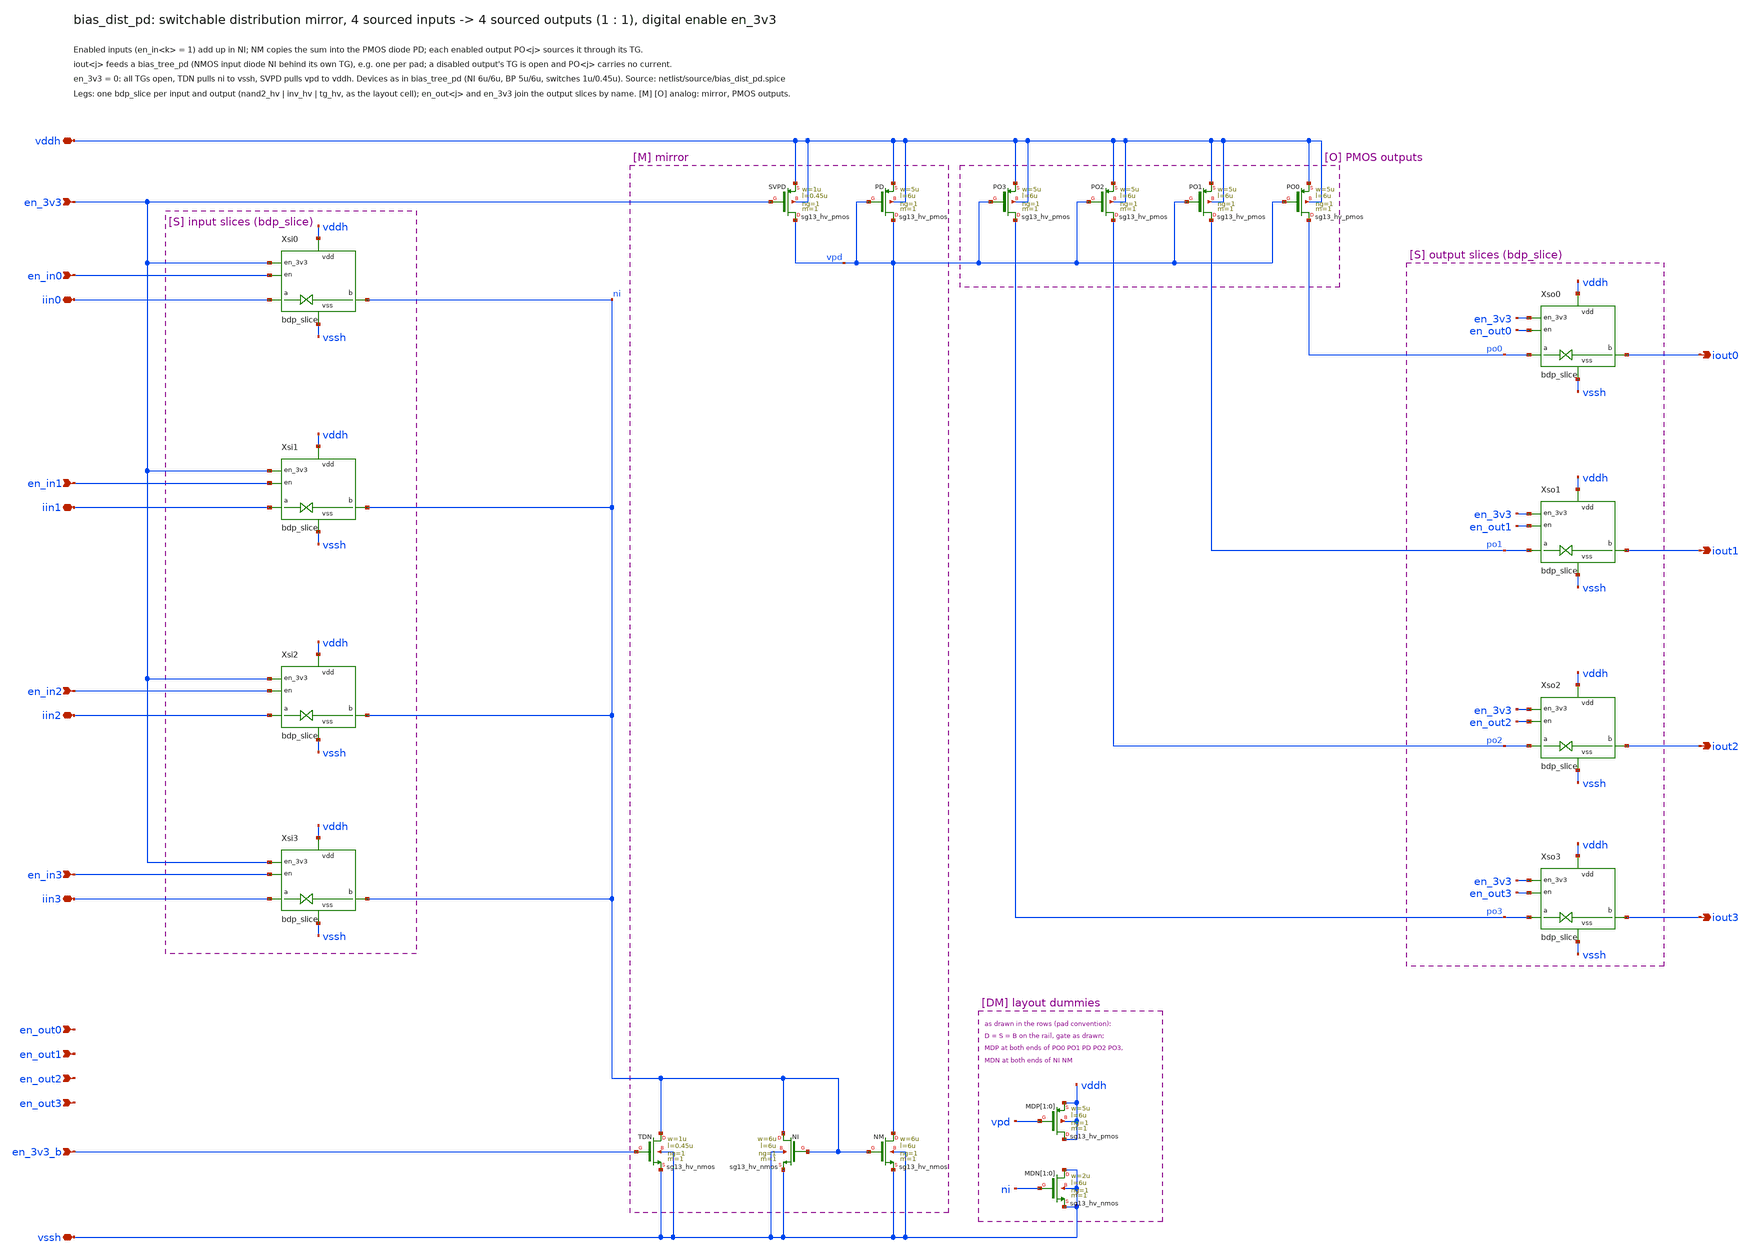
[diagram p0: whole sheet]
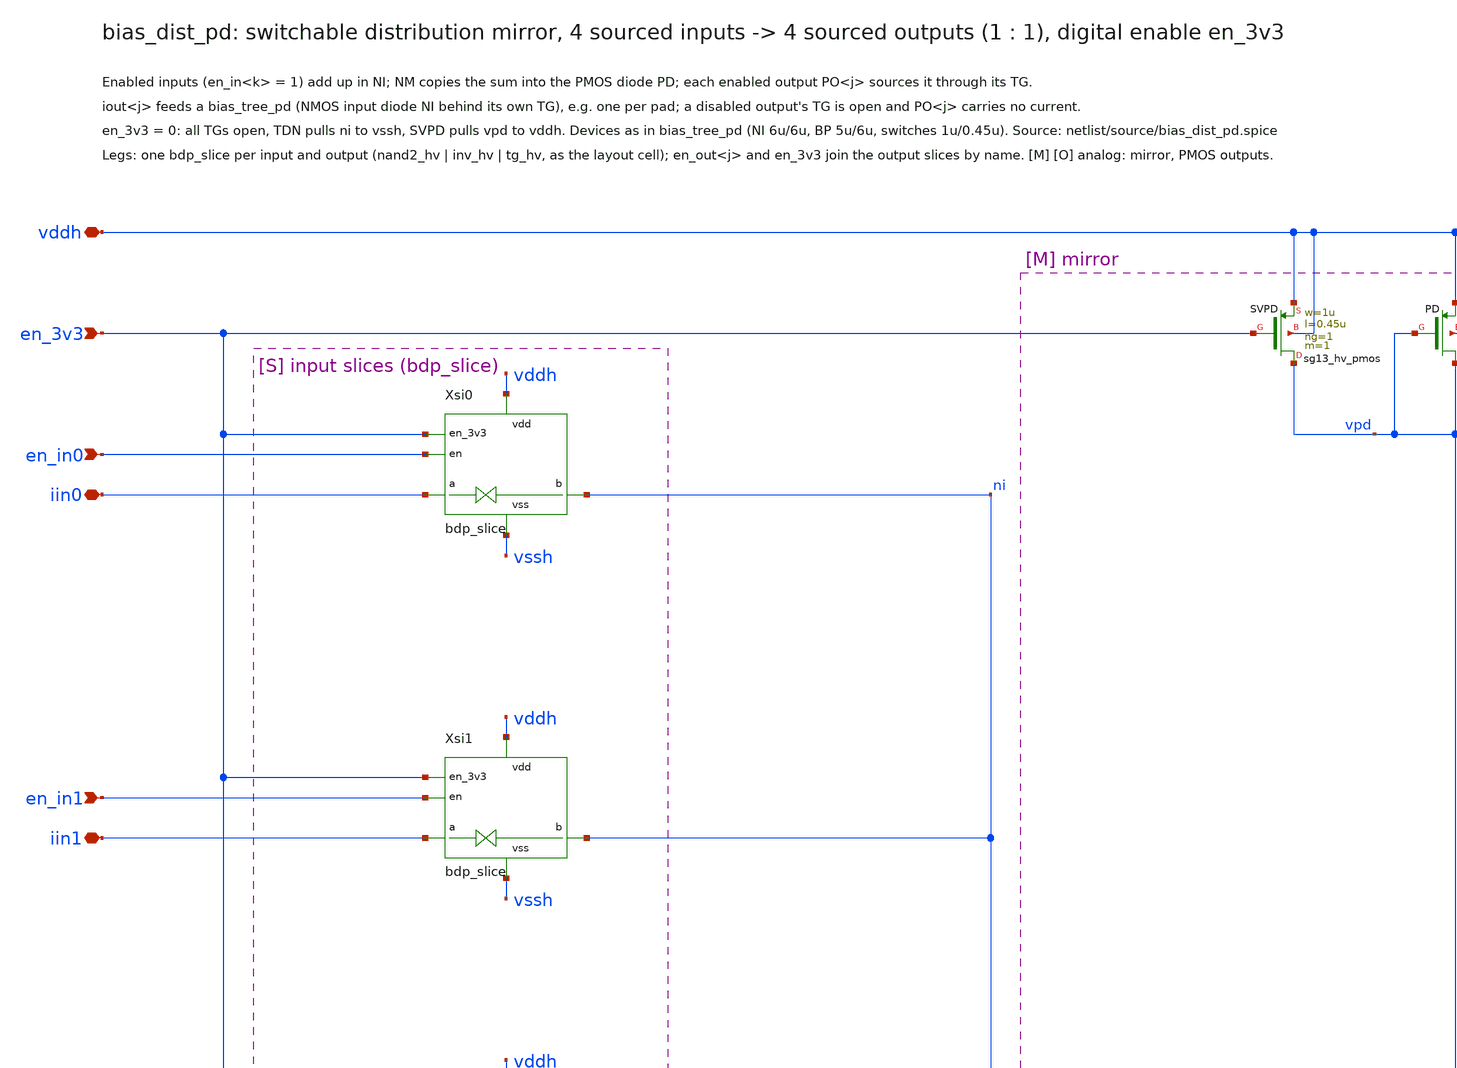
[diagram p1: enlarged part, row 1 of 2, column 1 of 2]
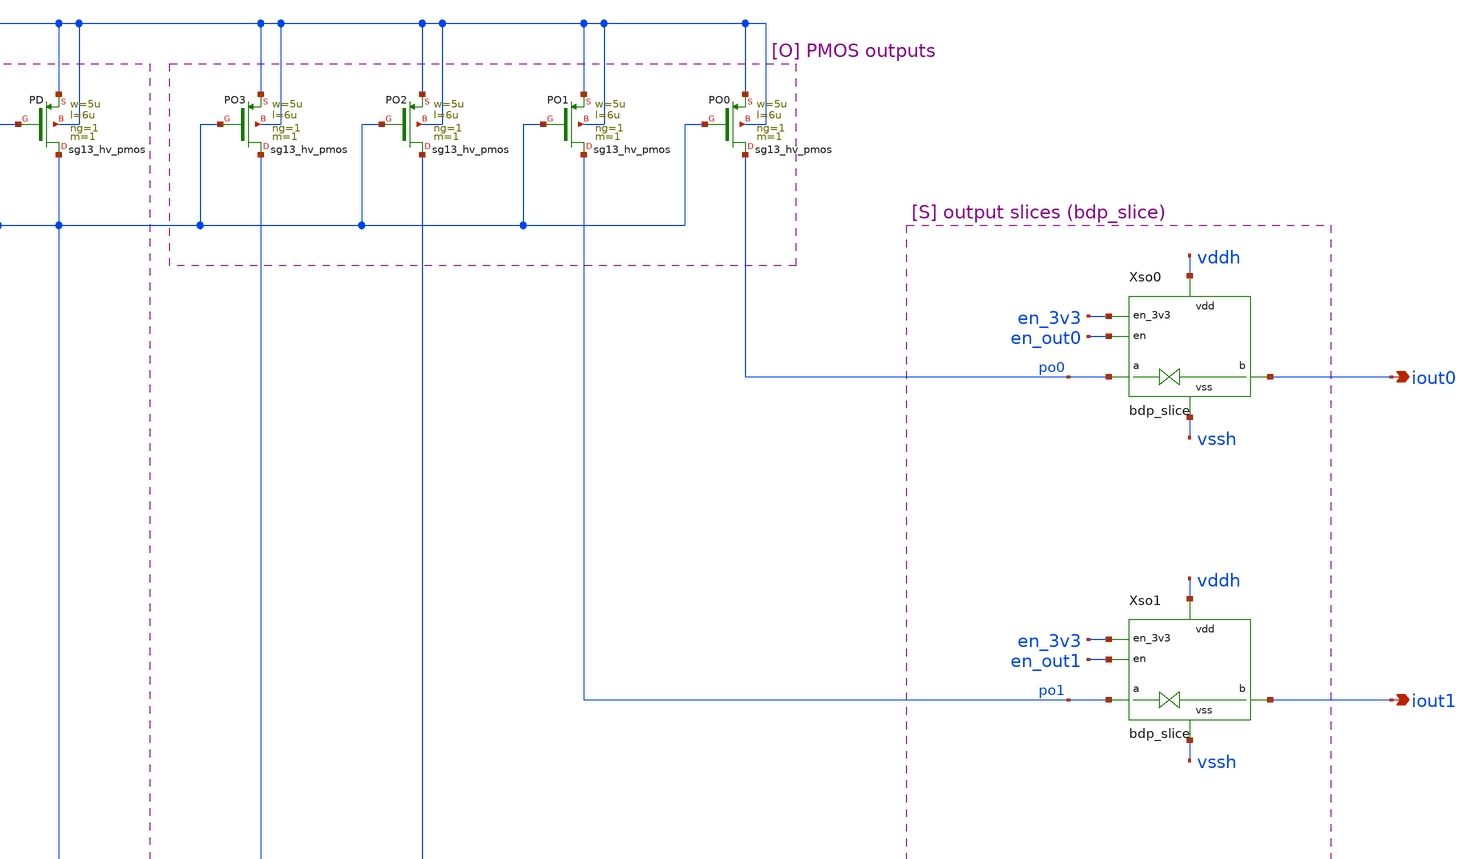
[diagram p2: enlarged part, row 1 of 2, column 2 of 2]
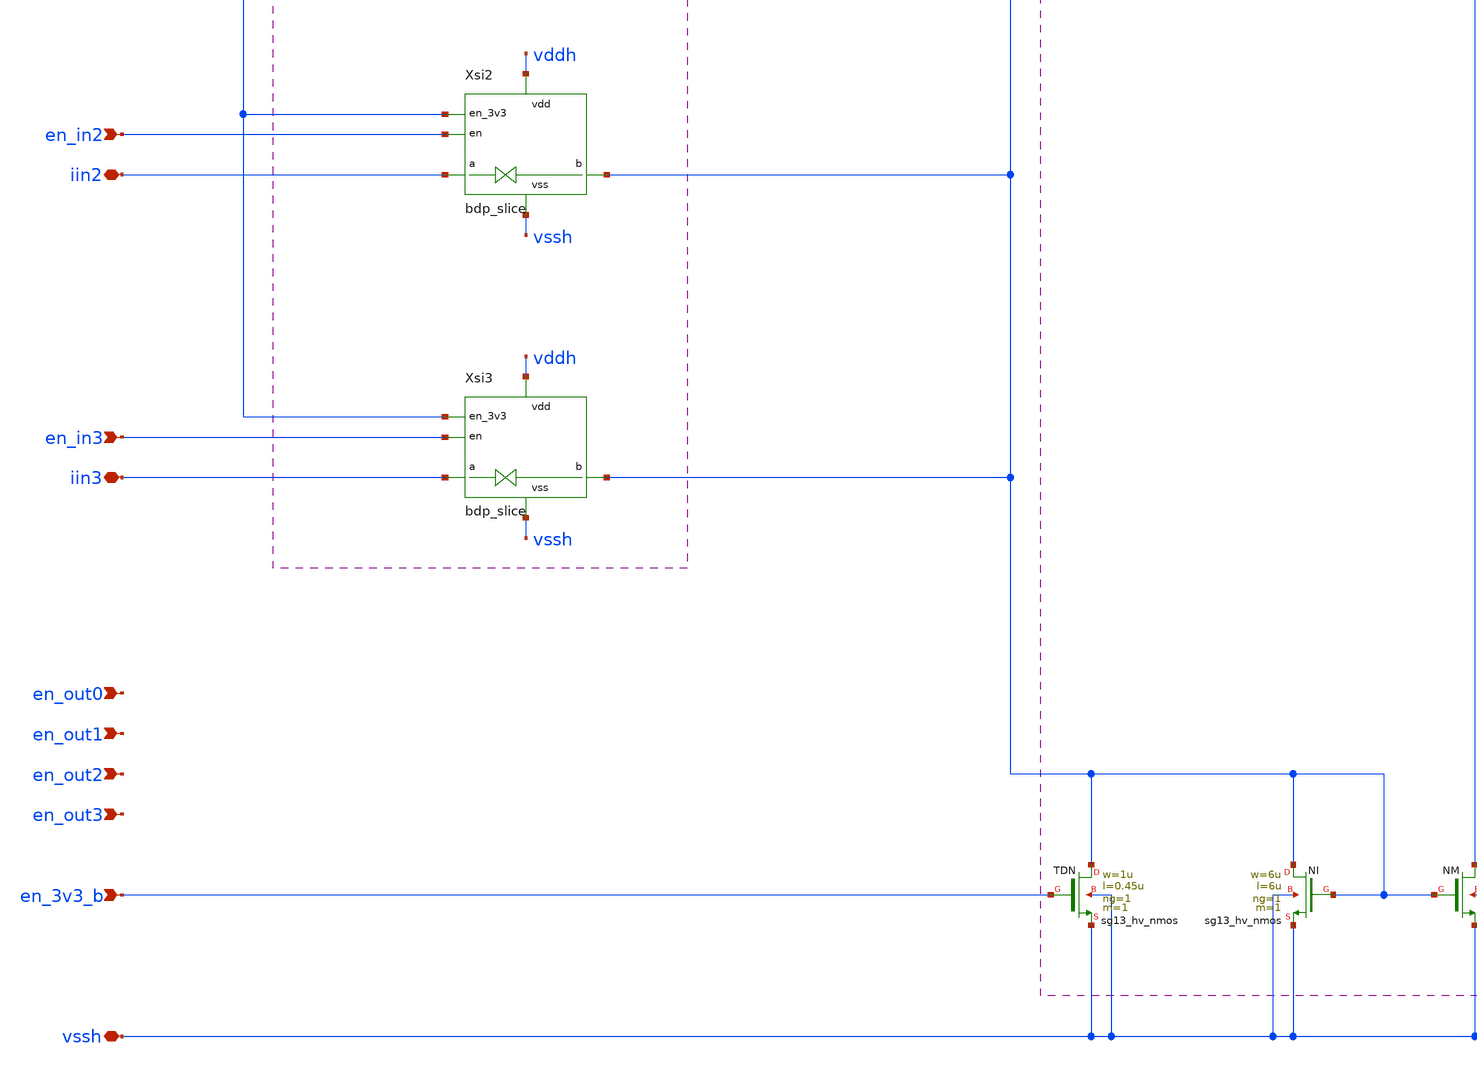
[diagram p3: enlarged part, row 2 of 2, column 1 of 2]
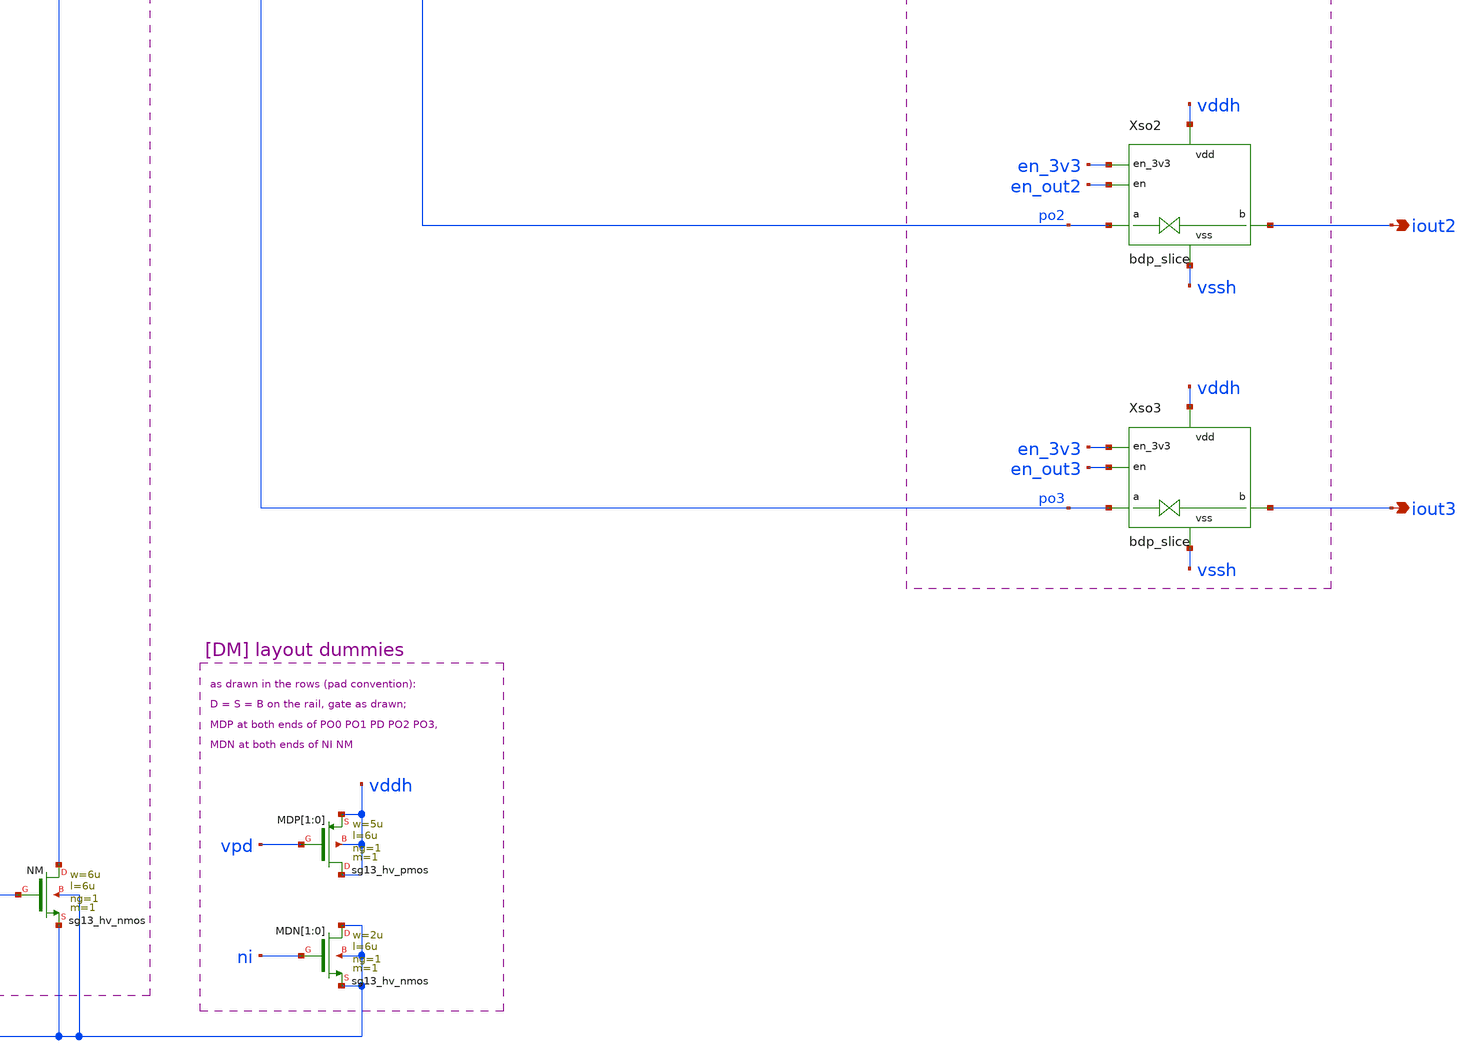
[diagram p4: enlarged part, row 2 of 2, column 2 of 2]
** sch_path: macros/bias_dist_pd/schematic/xschem/bias_dist_pd.sch
**.subckt bias_dist_pd vddh vssh en_3v3 en_3v3_b iin0 iin1 iin2 iin3 en_in0 en_in1 en_in2 en_in3
*+ iout0 iout1 iout2 iout3 en_out0 en_out1 en_out2 en_out3
*.iopin vddh
*.iopin vssh
*.ipin en_3v3
*.ipin en_3v3_b
*.iopin iin0
*.iopin iin1
*.iopin iin2
*.iopin iin3
*.ipin en_in0
*.ipin en_in1
*.ipin en_in2
*.ipin en_in3
*.opin iout0
*.opin iout1
*.opin iout2
*.opin iout3
*.ipin en_out0
*.ipin en_out1
*.ipin en_out2
*.ipin en_out3
XTDN ni en_3v3_b vssh vssh sg13_hv_nmos w=1u l=0.45u ng=1 m=1 mm_ok=1
XNI ni ni vssh vssh sg13_hv_nmos w=6u l=6u ng=1 m=1 mm_ok=1
XNM vpd ni vssh vssh sg13_hv_nmos w=6u l=6u ng=1 m=1 mm_ok=1
XPD vpd vpd vddh vddh sg13_hv_pmos w=5u l=6u ng=1 m=1 mm_ok=1
XSVPD vpd en_3v3 vddh vddh sg13_hv_pmos w=1u l=0.45u ng=1 m=1 mm_ok=1
XPO0 po0 vpd vddh vddh sg13_hv_pmos w=5u l=6u ng=1 m=1 mm_ok=1
XPO1 po1 vpd vddh vddh sg13_hv_pmos w=5u l=6u ng=1 m=1 mm_ok=1
XPO2 po2 vpd vddh vddh sg13_hv_pmos w=5u l=6u ng=1 m=1 mm_ok=1
XPO3 po3 vpd vddh vddh sg13_hv_pmos w=5u l=6u ng=1 m=1 mm_ok=1
XMDP[1] vddh vpd vddh vddh sg13_hv_pmos w=5u l=6u ng=1 m=1 mm_ok=1
XMDP[0] vddh vpd vddh vddh sg13_hv_pmos w=5u l=6u ng=1 m=1 mm_ok=1
XMDN[1] vssh ni vssh vssh sg13_hv_nmos w=2u l=6u ng=1 m=1 mm_ok=1
XMDN[0] vssh ni vssh vssh sg13_hv_nmos w=2u l=6u ng=1 m=1 mm_ok=1
Xsi0 vddh vssh en_3v3 en_in0 iin0 ni bdp_slice
Xsi1 vddh vssh en_3v3 en_in1 iin1 ni bdp_slice
Xsi2 vddh vssh en_3v3 en_in2 iin2 ni bdp_slice
Xsi3 vddh vssh en_3v3 en_in3 iin3 ni bdp_slice
Xso0 vddh vssh en_3v3 en_out0 po0 iout0 bdp_slice
Xso1 vddh vssh en_3v3 en_out1 po1 iout1 bdp_slice
Xso2 vddh vssh en_3v3 en_out2 po2 iout2 bdp_slice
Xso3 vddh vssh en_3v3 en_out3 po3 iout3 bdp_slice
**.ends

* expanding   symbol:  bdp_slice.sym # of pins=6
** sym_path: macros/bias_dist_pd/schematic/xschem/bdp_slice.sym
** sch_path: macros/bias_dist_pd/schematic/xschem/bdp_slice.sch
.subckt bdp_slice vdd vss en_3v3 en a b
*.iopin vdd
*.iopin vss
*.ipin en_3v3
*.ipin en
*.iopin a
*.iopin b
XA vdd vss en_3v3 en e_b nand2_hv
XB vdd vss e_b e inv_hv
XT vdd vss e e_b a b tg_hv
.ends


* expanding   symbol:  nand2_hv.sym # of pins=5
** sym_path: macros/hv_logic/schematic/xschem/nand2_hv.sym
** sch_path: macros/hv_logic/schematic/xschem/nand2_hv.sch
.subckt nand2_hv vdd vss a b y
*.iopin vdd
*.iopin vss
*.ipin a
*.ipin b
*.opin y
XPA y a vdd vdd sg13_hv_pmos w=1u l=0.45u ng=1 m=1 mm_ok=1
XPB y b vdd vdd sg13_hv_pmos w=1u l=0.45u ng=1 m=1 mm_ok=1
XNA y a n1 vss sg13_hv_nmos w=1u l=0.45u ng=1 m=1 mm_ok=1
XNB n1 b vss vss sg13_hv_nmos w=1u l=0.45u ng=1 m=1 mm_ok=1
.ends


* expanding   symbol:  inv_hv.sym # of pins=4
** sym_path: macros/hv_logic/schematic/xschem/inv_hv.sym
** sch_path: macros/hv_logic/schematic/xschem/inv_hv.sch
.subckt inv_hv vdd vss a y
*.iopin vdd
*.iopin vss
*.ipin a
*.opin y
XP y a vdd vdd sg13_hv_pmos w=1u l=0.45u ng=1 m=1 mm_ok=1
XN y a vss vss sg13_hv_nmos w=1u l=0.45u ng=1 m=1 mm_ok=1
.ends


* expanding   symbol:  tg_hv.sym # of pins=6
** sym_path: macros/hv_logic/schematic/xschem/tg_hv.sym
** sch_path: macros/hv_logic/schematic/xschem/tg_hv.sch
.subckt tg_hv vdd vss en en_b a b
*.iopin vdd
*.iopin vss
*.ipin en
*.ipin en_b
*.iopin a
*.iopin b
XN a en b vss sg13_hv_nmos w=1u l=0.45u ng=1 m=1 mm_ok=1
XP a en_b b vdd sg13_hv_pmos w=1u l=0.45u ng=1 m=1 mm_ok=1
.ends

.end
